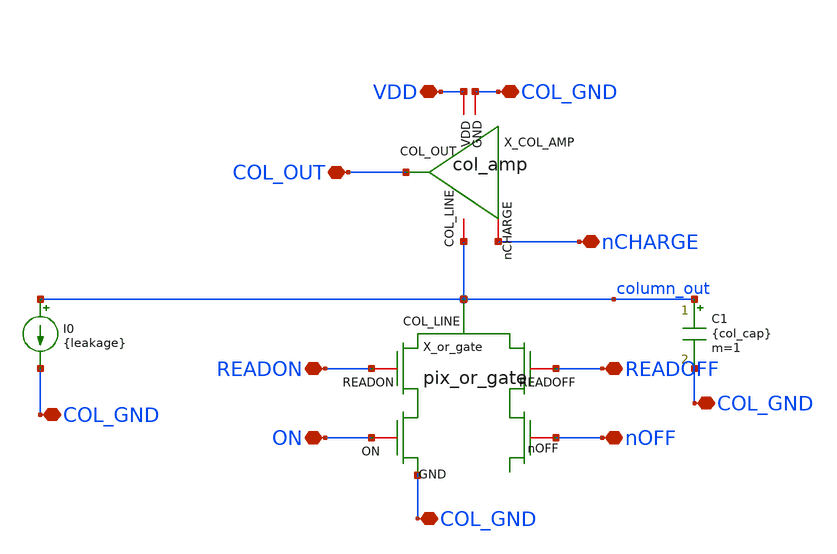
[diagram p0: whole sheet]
** sch_path: analog/xschem/col_amp_v2_std_dvs/xschem/TRAN_TF_TB.sch
**.subckt TRAN_TF_TB nCHARGE nOFF READOFF ON READON COL_GND COL_GND COL_GND VDD COL_OUT COL_GND
*.iopin nCHARGE
*.iopin nOFF
*.iopin READOFF
*.iopin ON
*.iopin READON
*.iopin COL_GND
*.iopin COL_GND
*.iopin COL_GND
*.iopin VDD
*.iopin COL_OUT
*.iopin COL_GND
X_COL_AMP VDD nCHARGE COL_OUT COL_GND column_out col_amp
C1 column_out COL_GND {col_cap} m=1
X_or_gate column_out READOFF READON nOFF ON COL_GND pix_or_gate
I0 column_out COL_GND {leakage}
**** begin user architecture code


.lib /home/alienfalcon/.ciel/sky130B/libs.tech/combined/sky130.lib.spice tt_mm

.option trtol=1 abstol=1p chgtol=4e-16 vntol=1e-9 reltol=1e-6
.option temp=27

.param vdd = 1.8
.param tr = 1p
.param tf = 1p
.param pw = 1u
.param col_cap = 300f
.param leakage = 5p

V_VDD VDD COL_GND DC {vdd}
V_GND COL_GND 0 DC 0
V_ON ON COL_GND DC {vdd}
V_nOFF nOFF COL_GND DC 0
V_READON READON COL_GND pulse(0 {vdd} {3*pw} {tr} {tf} {pw} {5*pw})
V_READOFF READOFF COL_GND DC 0
V_nCHARGE nCHARGE COL_GND pulse({vdd} 0 {pw} {tr} {tf} {pw} {5*pw})

.control
	option SEED=random
	let mc_runs = 100
	let run = 1
	let V_diff = 0
	let Vc_10 = 0
	let Vc_90 = 0
	let Vc_set_low = 0
	let Vc_set_high = 0
	let Vc_max = 0
	let Vc_min_rst = 0
	let Vc_max_rst = 0
	let Vc_min = 0
	let start_pulse = 4u
	let tset_col_setlow = 0
	let tset_col_high_trig = 0
	let tset_col_low_trig = 0
	let tf_col_out = 0

	save none

	op
	write TRAN_TF_TB.raw

	set appendwrite
	dowhile run <= mc_runs

		save v(COL_OUT) tset_col tf_col_out nosub nointernals
		optran 0 0 0 1p 10n 0
		tran 0.1n 5u

		set run = $&run

		meas tran Vc_max FIND v(COL_OUT) AT=1.3u
		meas tran Vc_max_rst FIND v(COL_OUT) AT=1.1u
		meas tran Vc_min FIND v(COL_OUT) AT=0.3u
		meas tran Vc_min_rst FIND v(COL_OUT) AT=3.1u
		let V_diff = Vc_max - Vc_min
		let Vc_mid = (Vc_max_rst + Vc_min_rst)/2
		let Vc_10 = V_diff*0.1 + Vc_min
		let Vc_90 = V_diff*0.9 + Vc_min
		let Vc_set_low = Vc_min*0.98
		let Vc_set_high = Vc_min*1.02

		*meas tran tr_col_out TRIG v(COL_OUT) VAL=Vc_10 CROSS=1 TARG v(COL_OUT) VAL=Vc_90 CROSS=1
		meas tran tf_col_out TRIG v(COL_OUT) VAL=Vc_90 FALL=LAST TARG v(COL_OUT) VAL=Vc_10 FALL=LAST
		meas tran tset_col_low WHEN v(COL_OUT)=Vc_set_low RISE=LAST
		meas tran tset_col_high WHEN v(COL_OUT)=Vc_set_high FALL=LAST

		let tset_col_setlow = ((tset_col_low + tset_col_high)/2) - start_pulse

		write TRAN_TF_TB.raw tset_col_setlow tf_col_out
		write TRAN_TF_TB.raw Vc_max_rst Vc_min_rst
		let run = run + 1
		reset
	end
	unset appendwrite
.endc




**** end user architecture code
**.ends
.end
